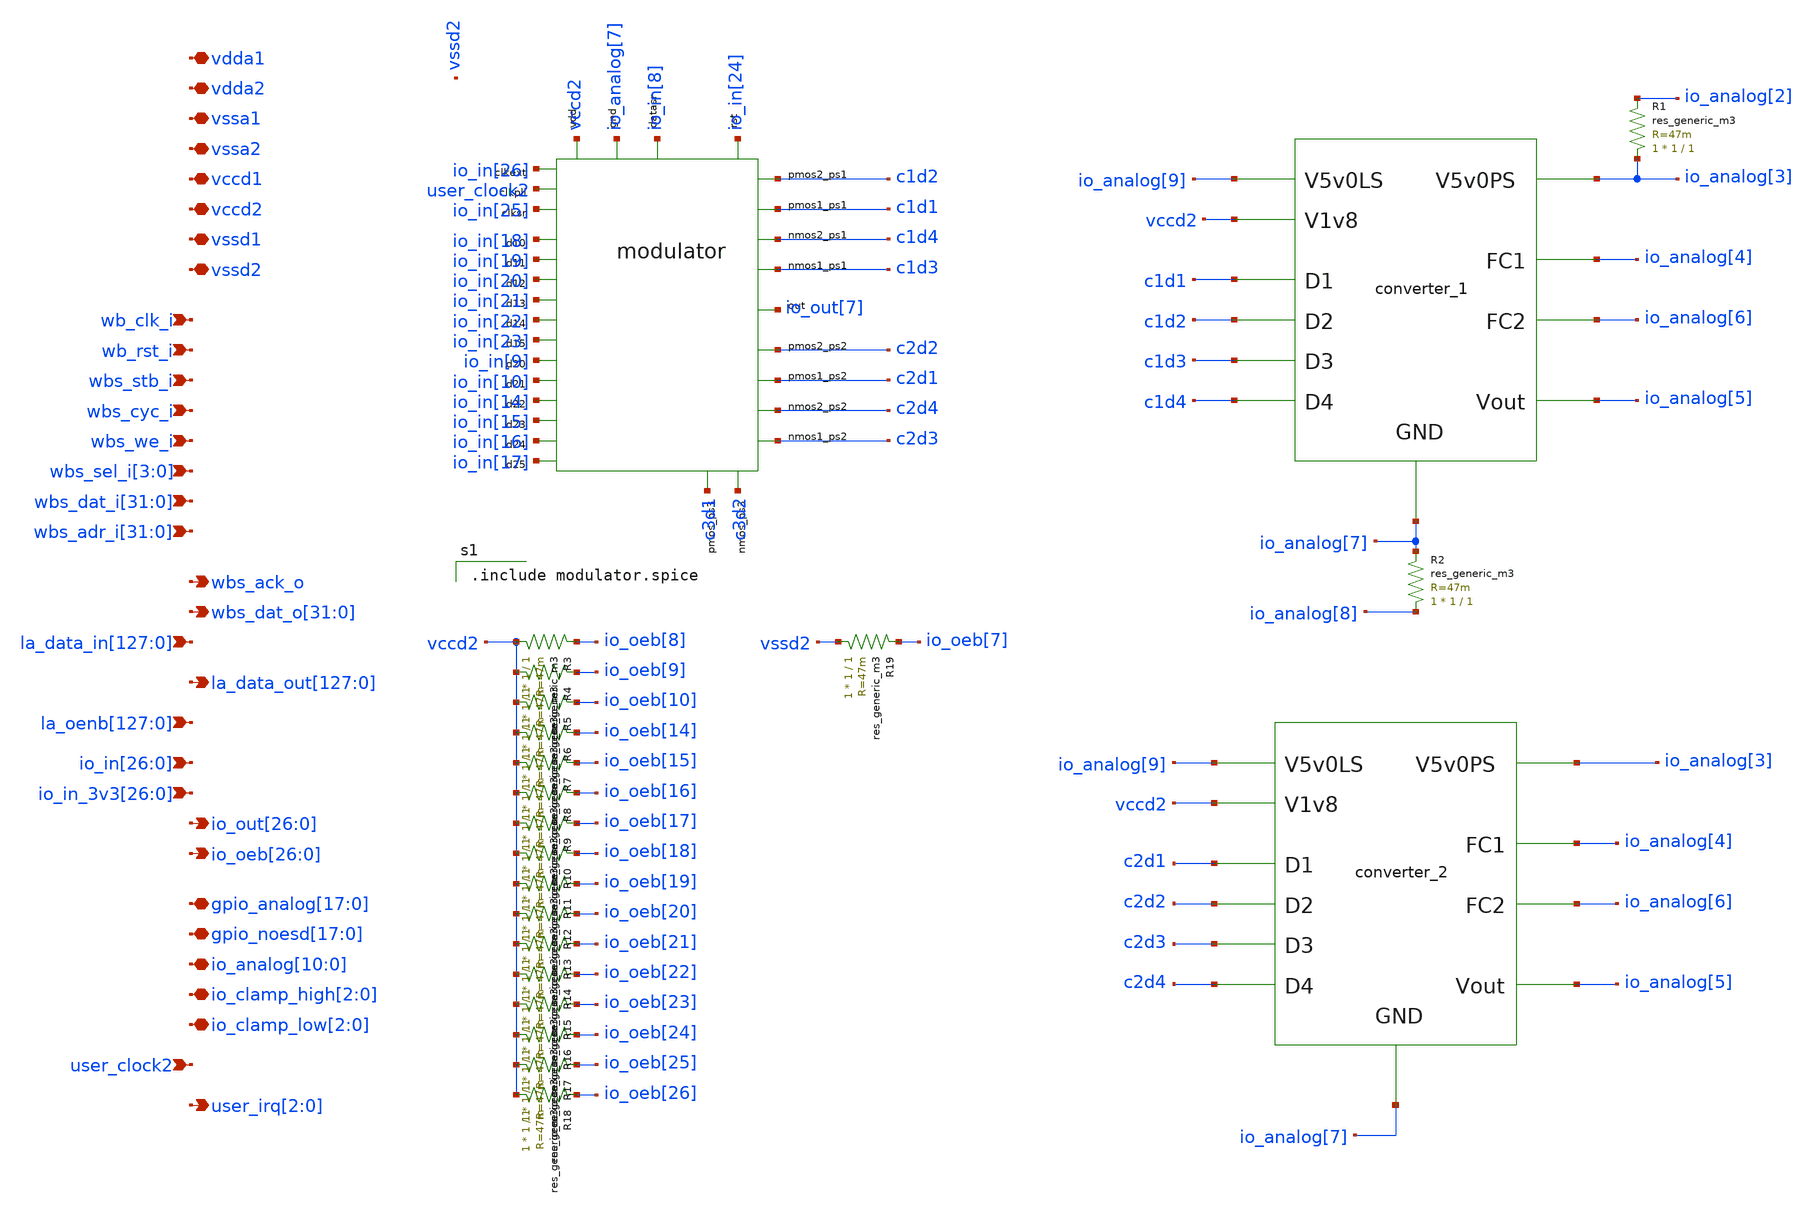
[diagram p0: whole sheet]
** sch_path: user_analog_project_wrapper.sch
**.subckt user_analog_project_wrapper vdda1 vdda2 vssa1 vssa2 vccd1 vccd2 vssd1 vssd2 wb_clk_i
*+ wb_rst_i wbs_stb_i wbs_cyc_i wbs_we_i wbs_sel_i[3],wbs_sel_i[2],wbs_sel_i[1],wbs_sel_i[0]
*+ wbs_dat_i[31],wbs_dat_i[30],wbs_dat_i[29],wbs_dat_i[28],wbs_dat_i[27],wbs_dat_i[26],wbs_dat_i[25],wbs_dat_i[24],wbs_dat_i[23],wbs_dat_i[22],wbs_dat_i[21],wbs_dat_i[20],wbs_dat_i[19],wbs_dat_i[18],wbs_dat_i[17],wbs_dat_i[16],wbs_dat_i[15],wbs_dat_i[14],wbs_dat_i[13],wbs_dat_i[12],wbs_dat_i[11],wbs_dat_i[10],wbs_dat_i[9],wbs_dat_i[8],wbs_dat_i[7],wbs_dat_i[6],wbs_dat_i[5],wbs_dat_i[4],wbs_dat_i[3],wbs_dat_i[2],wbs_dat_i[1],wbs_dat_i[0]
*+ wbs_adr_i[31],wbs_adr_i[30],wbs_adr_i[29],wbs_adr_i[28],wbs_adr_i[27],wbs_adr_i[26],wbs_adr_i[25],wbs_adr_i[24],wbs_adr_i[23],wbs_adr_i[22],wbs_adr_i[21],wbs_adr_i[20],wbs_adr_i[19],wbs_adr_i[18],wbs_adr_i[17],wbs_adr_i[16],wbs_adr_i[15],wbs_adr_i[14],wbs_adr_i[13],wbs_adr_i[12],wbs_adr_i[11],wbs_adr_i[10],wbs_adr_i[9],wbs_adr_i[8],wbs_adr_i[7],wbs_adr_i[6],wbs_adr_i[5],wbs_adr_i[4],wbs_adr_i[3],wbs_adr_i[2],wbs_adr_i[1],wbs_adr_i[0] wbs_ack_o
*+ wbs_dat_o[31],wbs_dat_o[30],wbs_dat_o[29],wbs_dat_o[28],wbs_dat_o[27],wbs_dat_o[26],wbs_dat_o[25],wbs_dat_o[24],wbs_dat_o[23],wbs_dat_o[22],wbs_dat_o[21],wbs_dat_o[20],wbs_dat_o[19],wbs_dat_o[18],wbs_dat_o[17],wbs_dat_o[16],wbs_dat_o[15],wbs_dat_o[14],wbs_dat_o[13],wbs_dat_o[12],wbs_dat_o[11],wbs_dat_o[10],wbs_dat_o[9],wbs_dat_o[8],wbs_dat_o[7],wbs_dat_o[6],wbs_dat_o[5],wbs_dat_o[4],wbs_dat_o[3],wbs_dat_o[2],wbs_dat_o[1],wbs_dat_o[0]
*+ la_data_in[127],la_data_in[126],la_data_in[125],la_data_in[124],la_data_in[123],la_data_in[122],la_data_in[121],la_data_in[120],la_data_in[119],la_data_in[118],la_data_in[117],la_data_in[116],la_data_in[115],la_data_in[114],la_data_in[113],la_data_in[112],la_data_in[111],la_data_in[110],la_data_in[109],la_data_in[108],la_data_in[107],la_data_in[106],la_data_in[105],la_data_in[104],la_data_in[103],la_data_in[102],la_data_in[101],la_data_in[100],la_data_in[99],la_data_in[98],la_data_in[97],la_data_in[96],la_data_in[95],la_data_in[94],la_data_in[93],la_data_in[92],la_data_in[91],la_data_in[90],la_data_in[89],la_data_in[88],la_data_in[87],la_data_in[86],la_data_in[85],la_data_in[84],la_data_in[83],la_data_in[82],la_data_in[81],la_data_in[80],la_data_in[79],la_data_in[78],la_data_in[77],la_data_in[76],la_data_in[75],la_data_in[74],la_data_in[73],la_data_in[72],la_data_in[71],la_data_in[70],la_data_in[69],la_data_in[68],la_data_in[67],la_data_in[66],la_data_in[65],la_data_in[64],la_data_in[63],la_data_in[62],la_data_in[61],la_data_in[60],la_data_in[59],la_data_in[58],la_data_in[57],la_data_in[56],la_data_in[55],la_data_in[54],la_data_in[53],la_data_in[52],la_data_in[51],la_data_in[50],la_data_in[49],la_data_in[48],la_data_in[47],la_data_in[46],la_data_in[45],la_data_in[44],la_data_in[43],la_data_in[42],la_data_in[41],la_data_in[40],la_data_in[39],la_data_in[38],la_data_in[37],la_data_in[36],la_data_in[35],la_data_in[34],la_data_in[33],la_data_in[32],la_data_in[31],la_data_in[30],la_data_in[29],la_data_in[28],la_data_in[27],la_data_in[26],la_data_in[25],la_data_in[24],la_data_in[23],la_data_in[22],la_data_in[21],la_data_in[20],la_data_in[19],la_data_in[18],la_data_in[17],la_data_in[16],la_data_in[15],la_data_in[14],la_data_in[13],la_data_in[12],la_data_in[11],la_data_in[10],la_data_in[9],la_data_in[8],la_data_in[7],la_data_in[6],la_data_in[5],la_data_in[4],la_data_in[3],la_data_in[2],la_data_in[1],la_data_in[0]
*+ la_data_out[127],la_data_out[126],la_data_out[125],la_data_out[124],la_data_out[123],la_data_out[122],la_data_out[121],la_data_out[120],la_data_out[119],la_data_out[118],la_data_out[117],la_data_out[116],la_data_out[115],la_data_out[114],la_data_out[113],la_data_out[112],la_data_out[111],la_data_out[110],la_data_out[109],la_data_out[108],la_data_out[107],la_data_out[106],la_data_out[105],la_data_out[104],la_data_out[103],la_data_out[102],la_data_out[101],la_data_out[100],la_data_out[99],la_data_out[98],la_data_out[97],la_data_out[96],la_data_out[95],la_data_out[94],la_data_out[93],la_data_out[92],la_data_out[91],la_data_out[90],la_data_out[89],la_data_out[88],la_data_out[87],la_data_out[86],la_data_out[85],la_data_out[84],la_data_out[83],la_data_out[82],la_data_out[81],la_data_out[80],la_data_out[79],la_data_out[78],la_data_out[77],la_data_out[76],la_data_out[75],la_data_out[74],la_data_out[73],la_data_out[72],la_data_out[71],la_data_out[70],la_data_out[69],la_data_out[68],la_data_out[67],la_data_out[66],la_data_out[65],la_data_out[64],la_data_out[63],la_data_out[62],la_data_out[61],la_data_out[60],la_data_out[59],la_data_out[58],la_data_out[57],la_data_out[56],la_data_out[55],la_data_out[54],la_data_out[53],la_data_out[52],la_data_out[51],la_data_out[50],la_data_out[49],la_data_out[48],la_data_out[47],la_data_out[46],la_data_out[45],la_data_out[44],la_data_out[43],la_data_out[42],la_data_out[41],la_data_out[40],la_data_out[39],la_data_out[38],la_data_out[37],la_data_out[36],la_data_out[35],la_data_out[34],la_data_out[33],la_data_out[32],la_data_out[31],la_data_out[30],la_data_out[29],la_data_out[28],la_data_out[27],la_data_out[26],la_data_out[25],la_data_out[24],la_data_out[23],la_data_out[22],la_data_out[21],la_data_out[20],la_data_out[19],la_data_out[18],la_data_out[17],la_data_out[16],la_data_out[15],la_data_out[14],la_data_out[13],la_data_out[12],la_data_out[11],la_data_out[10],la_data_out[9],la_data_out[8],la_data_out[7],la_data_out[6],la_data_out[5],la_data_out[4],la_data_out[3],la_data_out[2],la_data_out[1],la_data_out[0]
*+ io_in[26],io_in[25],io_in[24],io_in[23],io_in[22],io_in[21],io_in[20],io_in[19],io_in[18],io_in[17],io_in[16],io_in[15],io_in[14],io_in[13],io_in[12],io_in[11],io_in[10],io_in[9],io_in[8],io_in[7],io_in[6],io_in[5],io_in[4],io_in[3],io_in[2],io_in[1],io_in[0]
*+ io_in_3v3[26],io_in_3v3[25],io_in_3v3[24],io_in_3v3[23],io_in_3v3[22],io_in_3v3[21],io_in_3v3[20],io_in_3v3[19],io_in_3v3[18],io_in_3v3[17],io_in_3v3[16],io_in_3v3[15],io_in_3v3[14],io_in_3v3[13],io_in_3v3[12],io_in_3v3[11],io_in_3v3[10],io_in_3v3[9],io_in_3v3[8],io_in_3v3[7],io_in_3v3[6],io_in_3v3[5],io_in_3v3[4],io_in_3v3[3],io_in_3v3[2],io_in_3v3[1],io_in_3v3[0] user_clock2
*+ io_out[26],io_out[25],io_out[24],io_out[23],io_out[22],io_out[21],io_out[20],io_out[19],io_out[18],io_out[17],io_out[16],io_out[15],io_out[14],io_out[13],io_out[12],io_out[11],io_out[10],io_out[9],io_out[8],io_out[7],io_out[6],io_out[5],io_out[4],io_out[3],io_out[2],io_out[1],io_out[0]
*+ io_oeb[26],io_oeb[25],io_oeb[24],io_oeb[23],io_oeb[22],io_oeb[21],io_oeb[20],io_oeb[19],io_oeb[18],io_oeb[17],io_oeb[16],io_oeb[15],io_oeb[14],io_oeb[13],io_oeb[12],io_oeb[11],io_oeb[10],io_oeb[9],io_oeb[8],io_oeb[7],io_oeb[6],io_oeb[5],io_oeb[4],io_oeb[3],io_oeb[2],io_oeb[1],io_oeb[0]
*+ gpio_analog[17],gpio_analog[16],gpio_analog[15],gpio_analog[14],gpio_analog[13],gpio_analog[12],gpio_analog[11],gpio_analog[10],gpio_analog[9],gpio_analog[8],gpio_analog[7],gpio_analog[6],gpio_analog[5],gpio_analog[4],gpio_analog[3],gpio_analog[2],gpio_analog[1],gpio_analog[0]
*+ gpio_noesd[17],gpio_noesd[16],gpio_noesd[15],gpio_noesd[14],gpio_noesd[13],gpio_noesd[12],gpio_noesd[11],gpio_noesd[10],gpio_noesd[9],gpio_noesd[8],gpio_noesd[7],gpio_noesd[6],gpio_noesd[5],gpio_noesd[4],gpio_noesd[3],gpio_noesd[2],gpio_noesd[1],gpio_noesd[0]
*+ io_analog[10],io_analog[9],io_analog[8],io_analog[7],io_analog[6],io_analog[5],io_analog[4],io_analog[3],io_analog[2],io_analog[1],io_analog[0] io_clamp_high[2],io_clamp_high[1],io_clamp_high[0] io_clamp_low[2],io_clamp_low[1],io_clamp_low[0]
*+ user_irq[2],user_irq[1],user_irq[0]
*+ la_oenb[127],la_oenb[126],la_oenb[125],la_oenb[124],la_oenb[123],la_oenb[122],la_oenb[121],la_oenb[120],la_oenb[119],la_oenb[118],la_oenb[117],la_oenb[116],la_oenb[115],la_oenb[114],la_oenb[113],la_oenb[112],la_oenb[111],la_oenb[110],la_oenb[109],la_oenb[108],la_oenb[107],la_oenb[106],la_oenb[105],la_oenb[104],la_oenb[103],la_oenb[102],la_oenb[101],la_oenb[100],la_oenb[99],la_oenb[98],la_oenb[97],la_oenb[96],la_oenb[95],la_oenb[94],la_oenb[93],la_oenb[92],la_oenb[91],la_oenb[90],la_oenb[89],la_oenb[88],la_oenb[87],la_oenb[86],la_oenb[85],la_oenb[84],la_oenb[83],la_oenb[82],la_oenb[81],la_oenb[80],la_oenb[79],la_oenb[78],la_oenb[77],la_oenb[76],la_oenb[75],la_oenb[74],la_oenb[73],la_oenb[72],la_oenb[71],la_oenb[70],la_oenb[69],la_oenb[68],la_oenb[67],la_oenb[66],la_oenb[65],la_oenb[64],la_oenb[63],la_oenb[62],la_oenb[61],la_oenb[60],la_oenb[59],la_oenb[58],la_oenb[57],la_oenb[56],la_oenb[55],la_oenb[54],la_oenb[53],la_oenb[52],la_oenb[51],la_oenb[50],la_oenb[49],la_oenb[48],la_oenb[47],la_oenb[46],la_oenb[45],la_oenb[44],la_oenb[43],la_oenb[42],la_oenb[41],la_oenb[40],la_oenb[39],la_oenb[38],la_oenb[37],la_oenb[36],la_oenb[35],la_oenb[34],la_oenb[33],la_oenb[32],la_oenb[31],la_oenb[30],la_oenb[29],la_oenb[28],la_oenb[27],la_oenb[26],la_oenb[25],la_oenb[24],la_oenb[23],la_oenb[22],la_oenb[21],la_oenb[20],la_oenb[19],la_oenb[18],la_oenb[17],la_oenb[16],la_oenb[15],la_oenb[14],la_oenb[13],la_oenb[12],la_oenb[11],la_oenb[10],la_oenb[9],la_oenb[8],la_oenb[7],la_oenb[6],la_oenb[5],la_oenb[4],la_oenb[3],la_oenb[2],la_oenb[1],la_oenb[0]
*.iopin vdda1
*.iopin vdda2
*.iopin vssa1
*.iopin vssa2
*.iopin vccd1
*.iopin vccd2
*.iopin vssd1
*.iopin vssd2
*.ipin wb_clk_i
*.ipin wb_rst_i
*.ipin wbs_stb_i
*.ipin wbs_cyc_i
*.ipin wbs_we_i
*.ipin wbs_sel_i[3],wbs_sel_i[2],wbs_sel_i[1],wbs_sel_i[0]
*.ipin
*+ wbs_dat_i[31],wbs_dat_i[30],wbs_dat_i[29],wbs_dat_i[28],wbs_dat_i[27],wbs_dat_i[26],wbs_dat_i[25],wbs_dat_i[24],wbs_dat_i[23],wbs_dat_i[22],wbs_dat_i[21],wbs_dat_i[20],wbs_dat_i[19],wbs_dat_i[18],wbs_dat_i[17],wbs_dat_i[16],wbs_dat_i[15],wbs_dat_i[14],wbs_dat_i[13],wbs_dat_i[12],wbs_dat_i[11],wbs_dat_i[10],wbs_dat_i[9],wbs_dat_i[8],wbs_dat_i[7],wbs_dat_i[6],wbs_dat_i[5],wbs_dat_i[4],wbs_dat_i[3],wbs_dat_i[2],wbs_dat_i[1],wbs_dat_i[0]
*.ipin
*+ wbs_adr_i[31],wbs_adr_i[30],wbs_adr_i[29],wbs_adr_i[28],wbs_adr_i[27],wbs_adr_i[26],wbs_adr_i[25],wbs_adr_i[24],wbs_adr_i[23],wbs_adr_i[22],wbs_adr_i[21],wbs_adr_i[20],wbs_adr_i[19],wbs_adr_i[18],wbs_adr_i[17],wbs_adr_i[16],wbs_adr_i[15],wbs_adr_i[14],wbs_adr_i[13],wbs_adr_i[12],wbs_adr_i[11],wbs_adr_i[10],wbs_adr_i[9],wbs_adr_i[8],wbs_adr_i[7],wbs_adr_i[6],wbs_adr_i[5],wbs_adr_i[4],wbs_adr_i[3],wbs_adr_i[2],wbs_adr_i[1],wbs_adr_i[0]
*.opin wbs_ack_o
*.opin
*+ wbs_dat_o[31],wbs_dat_o[30],wbs_dat_o[29],wbs_dat_o[28],wbs_dat_o[27],wbs_dat_o[26],wbs_dat_o[25],wbs_dat_o[24],wbs_dat_o[23],wbs_dat_o[22],wbs_dat_o[21],wbs_dat_o[20],wbs_dat_o[19],wbs_dat_o[18],wbs_dat_o[17],wbs_dat_o[16],wbs_dat_o[15],wbs_dat_o[14],wbs_dat_o[13],wbs_dat_o[12],wbs_dat_o[11],wbs_dat_o[10],wbs_dat_o[9],wbs_dat_o[8],wbs_dat_o[7],wbs_dat_o[6],wbs_dat_o[5],wbs_dat_o[4],wbs_dat_o[3],wbs_dat_o[2],wbs_dat_o[1],wbs_dat_o[0]
*.ipin
*+ la_data_in[127],la_data_in[126],la_data_in[125],la_data_in[124],la_data_in[123],la_data_in[122],la_data_in[121],la_data_in[120],la_data_in[119],la_data_in[118],la_data_in[117],la_data_in[116],la_data_in[115],la_data_in[114],la_data_in[113],la_data_in[112],la_data_in[111],la_data_in[110],la_data_in[109],la_data_in[108],la_data_in[107],la_data_in[106],la_data_in[105],la_data_in[104],la_data_in[103],la_data_in[102],la_data_in[101],la_data_in[100],la_data_in[99],la_data_in[98],la_data_in[97],la_data_in[96],la_data_in[95],la_data_in[94],la_data_in[93],la_data_in[92],la_data_in[91],la_data_in[90],la_data_in[89],la_data_in[88],la_data_in[87],la_data_in[86],la_data_in[85],la_data_in[84],la_data_in[83],la_data_in[82],la_data_in[81],la_data_in[80],la_data_in[79],la_data_in[78],la_data_in[77],la_data_in[76],la_data_in[75],la_data_in[74],la_data_in[73],la_data_in[72],la_data_in[71],la_data_in[70],la_data_in[69],la_data_in[68],la_data_in[67],la_data_in[66],la_data_in[65],la_data_in[64],la_data_in[63],la_data_in[62],la_data_in[61],la_data_in[60],la_data_in[59],la_data_in[58],la_data_in[57],la_data_in[56],la_data_in[55],la_data_in[54],la_data_in[53],la_data_in[52],la_data_in[51],la_data_in[50],la_data_in[49],la_data_in[48],la_data_in[47],la_data_in[46],la_data_in[45],la_data_in[44],la_data_in[43],la_data_in[42],la_data_in[41],la_data_in[40],la_data_in[39],la_data_in[38],la_data_in[37],la_data_in[36],la_data_in[35],la_data_in[34],la_data_in[33],la_data_in[32],la_data_in[31],la_data_in[30],la_data_in[29],la_data_in[28],la_data_in[27],la_data_in[26],la_data_in[25],la_data_in[24],la_data_in[23],la_data_in[22],la_data_in[21],la_data_in[20],la_data_in[19],la_data_in[18],la_data_in[17],la_data_in[16],la_data_in[15],la_data_in[14],la_data_in[13],la_data_in[12],la_data_in[11],la_data_in[10],la_data_in[9],la_data_in[8],la_data_in[7],la_data_in[6],la_data_in[5],la_data_in[4],la_data_in[3],la_data_in[2],la_data_in[1],la_data_in[0]
*.opin
*+ la_data_out[127],la_data_out[126],la_data_out[125],la_data_out[124],la_data_out[123],la_data_out[122],la_data_out[121],la_data_out[120],la_data_out[119],la_data_out[118],la_data_out[117],la_data_out[116],la_data_out[115],la_data_out[114],la_data_out[113],la_data_out[112],la_data_out[111],la_data_out[110],la_data_out[109],la_data_out[108],la_data_out[107],la_data_out[106],la_data_out[105],la_data_out[104],la_data_out[103],la_data_out[102],la_data_out[101],la_data_out[100],la_data_out[99],la_data_out[98],la_data_out[97],la_data_out[96],la_data_out[95],la_data_out[94],la_data_out[93],la_data_out[92],la_data_out[91],la_data_out[90],la_data_out[89],la_data_out[88],la_data_out[87],la_data_out[86],la_data_out[85],la_data_out[84],la_data_out[83],la_data_out[82],la_data_out[81],la_data_out[80],la_data_out[79],la_data_out[78],la_data_out[77],la_data_out[76],la_data_out[75],la_data_out[74],la_data_out[73],la_data_out[72],la_data_out[71],la_data_out[70],la_data_out[69],la_data_out[68],la_data_out[67],la_data_out[66],la_data_out[65],la_data_out[64],la_data_out[63],la_data_out[62],la_data_out[61],la_data_out[60],la_data_out[59],la_data_out[58],la_data_out[57],la_data_out[56],la_data_out[55],la_data_out[54],la_data_out[53],la_data_out[52],la_data_out[51],la_data_out[50],la_data_out[49],la_data_out[48],la_data_out[47],la_data_out[46],la_data_out[45],la_data_out[44],la_data_out[43],la_data_out[42],la_data_out[41],la_data_out[40],la_data_out[39],la_data_out[38],la_data_out[37],la_data_out[36],la_data_out[35],la_data_out[34],la_data_out[33],la_data_out[32],la_data_out[31],la_data_out[30],la_data_out[29],la_data_out[28],la_data_out[27],la_data_out[26],la_data_out[25],la_data_out[24],la_data_out[23],la_data_out[22],la_data_out[21],la_data_out[20],la_data_out[19],la_data_out[18],la_data_out[17],la_data_out[16],la_data_out[15],la_data_out[14],la_data_out[13],la_data_out[12],la_data_out[11],la_data_out[10],la_data_out[9],la_data_out[8],la_data_out[7],la_data_out[6],la_data_out[5],la_data_out[4],la_data_out[3],la_data_out[2],la_data_out[1],la_data_out[0]
*.ipin
*+ io_in[26],io_in[25],io_in[24],io_in[23],io_in[22],io_in[21],io_in[20],io_in[19],io_in[18],io_in[17],io_in[16],io_in[15],io_in[14],io_in[13],io_in[12],io_in[11],io_in[10],io_in[9],io_in[8],io_in[7],io_in[6],io_in[5],io_in[4],io_in[3],io_in[2],io_in[1],io_in[0]
*.ipin
*+ io_in_3v3[26],io_in_3v3[25],io_in_3v3[24],io_in_3v3[23],io_in_3v3[22],io_in_3v3[21],io_in_3v3[20],io_in_3v3[19],io_in_3v3[18],io_in_3v3[17],io_in_3v3[16],io_in_3v3[15],io_in_3v3[14],io_in_3v3[13],io_in_3v3[12],io_in_3v3[11],io_in_3v3[10],io_in_3v3[9],io_in_3v3[8],io_in_3v3[7],io_in_3v3[6],io_in_3v3[5],io_in_3v3[4],io_in_3v3[3],io_in_3v3[2],io_in_3v3[1],io_in_3v3[0]
*.ipin user_clock2
*.opin
*+ io_out[26],io_out[25],io_out[24],io_out[23],io_out[22],io_out[21],io_out[20],io_out[19],io_out[18],io_out[17],io_out[16],io_out[15],io_out[14],io_out[13],io_out[12],io_out[11],io_out[10],io_out[9],io_out[8],io_out[7],io_out[6],io_out[5],io_out[4],io_out[3],io_out[2],io_out[1],io_out[0]
*.opin
*+ io_oeb[26],io_oeb[25],io_oeb[24],io_oeb[23],io_oeb[22],io_oeb[21],io_oeb[20],io_oeb[19],io_oeb[18],io_oeb[17],io_oeb[16],io_oeb[15],io_oeb[14],io_oeb[13],io_oeb[12],io_oeb[11],io_oeb[10],io_oeb[9],io_oeb[8],io_oeb[7],io_oeb[6],io_oeb[5],io_oeb[4],io_oeb[3],io_oeb[2],io_oeb[1],io_oeb[0]
*.iopin
*+ gpio_analog[17],gpio_analog[16],gpio_analog[15],gpio_analog[14],gpio_analog[13],gpio_analog[12],gpio_analog[11],gpio_analog[10],gpio_analog[9],gpio_analog[8],gpio_analog[7],gpio_analog[6],gpio_analog[5],gpio_analog[4],gpio_analog[3],gpio_analog[2],gpio_analog[1],gpio_analog[0]
*.iopin
*+ gpio_noesd[17],gpio_noesd[16],gpio_noesd[15],gpio_noesd[14],gpio_noesd[13],gpio_noesd[12],gpio_noesd[11],gpio_noesd[10],gpio_noesd[9],gpio_noesd[8],gpio_noesd[7],gpio_noesd[6],gpio_noesd[5],gpio_noesd[4],gpio_noesd[3],gpio_noesd[2],gpio_noesd[1],gpio_noesd[0]
*.iopin
*+ io_analog[10],io_analog[9],io_analog[8],io_analog[7],io_analog[6],io_analog[5],io_analog[4],io_analog[3],io_analog[2],io_analog[1],io_analog[0]
*.iopin io_clamp_high[2],io_clamp_high[1],io_clamp_high[0]
*.iopin io_clamp_low[2],io_clamp_low[1],io_clamp_low[0]
*.opin user_irq[2],user_irq[1],user_irq[0]
*.ipin
*+ la_oenb[127],la_oenb[126],la_oenb[125],la_oenb[124],la_oenb[123],la_oenb[122],la_oenb[121],la_oenb[120],la_oenb[119],la_oenb[118],la_oenb[117],la_oenb[116],la_oenb[115],la_oenb[114],la_oenb[113],la_oenb[112],la_oenb[111],la_oenb[110],la_oenb[109],la_oenb[108],la_oenb[107],la_oenb[106],la_oenb[105],la_oenb[104],la_oenb[103],la_oenb[102],la_oenb[101],la_oenb[100],la_oenb[99],la_oenb[98],la_oenb[97],la_oenb[96],la_oenb[95],la_oenb[94],la_oenb[93],la_oenb[92],la_oenb[91],la_oenb[90],la_oenb[89],la_oenb[88],la_oenb[87],la_oenb[86],la_oenb[85],la_oenb[84],la_oenb[83],la_oenb[82],la_oenb[81],la_oenb[80],la_oenb[79],la_oenb[78],la_oenb[77],la_oenb[76],la_oenb[75],la_oenb[74],la_oenb[73],la_oenb[72],la_oenb[71],la_oenb[70],la_oenb[69],la_oenb[68],la_oenb[67],la_oenb[66],la_oenb[65],la_oenb[64],la_oenb[63],la_oenb[62],la_oenb[61],la_oenb[60],la_oenb[59],la_oenb[58],la_oenb[57],la_oenb[56],la_oenb[55],la_oenb[54],la_oenb[53],la_oenb[52],la_oenb[51],la_oenb[50],la_oenb[49],la_oenb[48],la_oenb[47],la_oenb[46],la_oenb[45],la_oenb[44],la_oenb[43],la_oenb[42],la_oenb[41],la_oenb[40],la_oenb[39],la_oenb[38],la_oenb[37],la_oenb[36],la_oenb[35],la_oenb[34],la_oenb[33],la_oenb[32],la_oenb[31],la_oenb[30],la_oenb[29],la_oenb[28],la_oenb[27],la_oenb[26],la_oenb[25],la_oenb[24],la_oenb[23],la_oenb[22],la_oenb[21],la_oenb[20],la_oenb[19],la_oenb[18],la_oenb[17],la_oenb[16],la_oenb[15],la_oenb[14],la_oenb[13],la_oenb[12],la_oenb[11],la_oenb[10],la_oenb[9],la_oenb[8],la_oenb[7],la_oenb[6],la_oenb[5],la_oenb[4],la_oenb[3],la_oenb[2],la_oenb[1],la_oenb[0]
X1 vccd2 c1d2 c1d1 io_analog[3] io_analog[7] io_analog[5] c1d3 c1d4 io_analog[4] io_analog[6]
+ io_analog[9] converter_1
X2 vccd2 c2d2 c2d1 io_analog[3] io_analog[7] io_analog[5] c2d3 c2d4 io_analog[4] io_analog[6]
+ io_analog[9] converter_2
XMOD1 vccd2 io_analog[7] io_in[26] user_clock2 io_in[25] io_in[8] c1d3 c2d3 c1d4 c2d4 c3d2 c1d1 c2d1
+ c1d2 c2d2 c3d1 io_in[24] io_out[7] io_in[18] io_in[19] io_in[20] io_in[21] io_in[22] io_in[23] io_in[9]
+ io_in[10] io_in[14] io_in[15] io_in[16] io_in[17] Modulator
R1 io_analog[3] io_analog[2] sky130_fd_pr__res_generic_m3 W=1 L=1 m=1
R2 io_analog[8] io_analog[7] sky130_fd_pr__res_generic_m3 W=1 L=1 m=1
R3 vccd2 io_oeb[8] sky130_fd_pr__res_generic_m3 W=1 L=1 m=1
R4 vccd2 io_oeb[9] sky130_fd_pr__res_generic_m3 W=1 L=1 m=1
R5 vccd2 io_oeb[10] sky130_fd_pr__res_generic_m3 W=1 L=1 m=1
R6 vccd2 io_oeb[14] sky130_fd_pr__res_generic_m3 W=1 L=1 m=1
R7 vccd2 io_oeb[15] sky130_fd_pr__res_generic_m3 W=1 L=1 m=1
R8 vccd2 io_oeb[16] sky130_fd_pr__res_generic_m3 W=1 L=1 m=1
R9 vccd2 io_oeb[17] sky130_fd_pr__res_generic_m3 W=1 L=1 m=1
R10 vccd2 io_oeb[18] sky130_fd_pr__res_generic_m3 W=1 L=1 m=1
R11 vccd2 io_oeb[19] sky130_fd_pr__res_generic_m3 W=1 L=1 m=1
R12 vccd2 io_oeb[20] sky130_fd_pr__res_generic_m3 W=1 L=1 m=1
R13 vccd2 io_oeb[21] sky130_fd_pr__res_generic_m3 W=1 L=1 m=1
R14 vccd2 io_oeb[22] sky130_fd_pr__res_generic_m3 W=1 L=1 m=1
R15 vccd2 io_oeb[23] sky130_fd_pr__res_generic_m3 W=1 L=1 m=1
R16 vccd2 io_oeb[24] sky130_fd_pr__res_generic_m3 W=1 L=1 m=1
R17 vccd2 io_oeb[25] sky130_fd_pr__res_generic_m3 W=1 L=1 m=1
R18 vccd2 io_oeb[26] sky130_fd_pr__res_generic_m3 W=1 L=1 m=1
R19 vssd2 io_oeb[7] sky130_fd_pr__res_generic_m3 W=1 L=1 m=1
**** begin user architecture code

.include modulator.spice

**** end user architecture code
**.ends

* expanding   symbol:  converter_1.sym # of pins=11
** sym_path: converter_1.sym
** sch_path: converter_1.sch
.subckt converter_1 V1v8 D2 D1 V5v0PS GND VOUT D3 D4 FC1 FC2 V5v0LS
*.iopin V5v0PS
*.ipin D2
*.ipin D3
*.ipin D4
*.iopin GND
*.iopin V5v0LS
*.iopin FC1
*.iopin FC2
*.iopin V1v8
*.ipin D1
*.iopin VOUT
x4 V5v0LS V1v8 net4 D4 GND level_shifter
x3 V5v0LS V1v8 net3 D3 GND level_shifter
x2 V5v0LS V1v8 net2 D2 GND level_shifter
x1 V5v0LS V1v8 net1 D1 GND level_shifter
X5 net1 net2 net3 net4 FC1 FC2 VOUT V5v0PS GND power_stage_1
.ends


* expanding   symbol:  converter_2.sym # of pins=11
** sym_path: converter_2.sym
** sch_path: converter_2.sch
.subckt converter_2 V1v8 D2 D1 V5v0PS GND VOUT D3 D4 FC1 FC2 V5v0LS
*.iopin V5v0PS
*.ipin D1
*.ipin D2
*.ipin D3
*.ipin D4
*.iopin V1v8
*.iopin GND
*.iopin V5v0LS
*.iopin FC1
*.iopin FC2
*.iopin VOUT
x4 V5v0LS V1v8 net4 D4 GND level_shifter
x3 V5v0LS V1v8 net3 D3 GND level_shifter
x2 V5v0LS V1v8 net2 D2 GND level_shifter
x1 V5v0LS V1v8 net1 D1 GND level_shifter
X5 net1 net2 net3 net4 FC1 FC2 VOUT V5v0PS GND power_stage_2
.ends


* expanding   symbol:  level_shifter.sym # of pins=5
** sym_path: level_shifter.sym
** sch_path: level_shifter.sch
.subckt level_shifter V5v0 V1v8 OUT IN V0v0
*.ipin IN
*.iopin V1v8
*.iopin V5v0
*.opin OUT
*.iopin V0v0
XM11 net1 IN V1v8 V1v8 sky130_fd_pr__pfet_01v8 L=0.15 W=1 nf=1 ad='int((nf+1)/2) * W/nf * 0.29' as='int((nf+2)/2) * W/nf * 0.29'
+ pd='2*int((nf+1)/2) * (W/nf + 0.29)' ps='2*int((nf+2)/2) * (W/nf + 0.29)' nrd='0.29 / W' nrs='0.29 / W'
+ sa=0 sb=0 sd=0 mult=5 m=5
XM12 net1 IN V0v0 V0v0 sky130_fd_pr__nfet_01v8 L=0.15 W=1 nf=1 ad='int((nf+1)/2) * W/nf * 0.29' as='int((nf+2)/2) * W/nf * 0.29'
+ pd='2*int((nf+1)/2) * (W/nf + 0.29)' ps='2*int((nf+2)/2) * (W/nf + 0.29)' nrd='0.29 / W' nrs='0.29 / W'
+ sa=0 sb=0 sd=0 mult=5 m=5
XM15 net2 net3 V5v0 V5v0 sky130_fd_pr__pfet_g5v0d10v5 L=0.5 W=2 nf=1 ad='int((nf+1)/2) * W/nf * 0.29'
+ as='int((nf+2)/2) * W/nf * 0.29' pd='2*int((nf+1)/2) * (W/nf + 0.29)' ps='2*int((nf+2)/2) * (W/nf + 0.29)'
+ nrd='0.29 / W' nrs='0.29 / W' sa=0 sb=0 sd=0 mult=1 m=1
XM14 net3 net2 V5v0 V5v0 sky130_fd_pr__pfet_g5v0d10v5 L=0.5 W=2 nf=1 ad='int((nf+1)/2) * W/nf * 0.29'
+ as='int((nf+2)/2) * W/nf * 0.29' pd='2*int((nf+1)/2) * (W/nf + 0.29)' ps='2*int((nf+2)/2) * (W/nf + 0.29)'
+ nrd='0.29 / W' nrs='0.29 / W' sa=0 sb=0 sd=0 mult=1 m=1
XM16 net4 net2 V5v0 V5v0 sky130_fd_pr__pfet_g5v0d10v5 L=0.5 W=10 nf=1 ad='int((nf+1)/2) * W/nf * 0.29'
+ as='int((nf+2)/2) * W/nf * 0.29' pd='2*int((nf+1)/2) * (W/nf + 0.29)' ps='2*int((nf+2)/2) * (W/nf + 0.29)'
+ nrd='0.29 / W' nrs='0.29 / W' sa=0 sb=0 sd=0 mult=10 m=10
XM18 net2 net1 V0v0 V0v0 sky130_fd_pr__nfet_g5v0d10v5 L=0.5 W=4 nf=1 ad='int((nf+1)/2) * W/nf * 0.29'
+ as='int((nf+2)/2) * W/nf * 0.29' pd='2*int((nf+1)/2) * (W/nf + 0.29)' ps='2*int((nf+2)/2) * (W/nf + 0.29)'
+ nrd='0.29 / W' nrs='0.29 / W' sa=0 sb=0 sd=0 mult=3 m=3
XM13 net3 IN V0v0 V0v0 sky130_fd_pr__nfet_g5v0d10v5 L=0.5 W=4 nf=1 ad='int((nf+1)/2) * W/nf * 0.29' as='int((nf+2)/2) * W/nf * 0.29'
+ pd='2*int((nf+1)/2) * (W/nf + 0.29)' ps='2*int((nf+2)/2) * (W/nf + 0.29)' nrd='0.29 / W' nrs='0.29 / W'
+ sa=0 sb=0 sd=0 mult=3 m=3
XM17 net4 IN V0v0 V0v0 sky130_fd_pr__nfet_g5v0d10v5 L=0.5 W=10 nf=1 ad='int((nf+1)/2) * W/nf * 0.29'
+ as='int((nf+2)/2) * W/nf * 0.29' pd='2*int((nf+1)/2) * (W/nf + 0.29)' ps='2*int((nf+2)/2) * (W/nf + 0.29)'
+ nrd='0.29 / W' nrs='0.29 / W' sa=0 sb=0 sd=0 mult=10 m=10
XM7 OUT net4 V5v0 V5v0 sky130_fd_pr__pfet_g5v0d10v5 L=0.5 W=20 nf=1 ad='int((nf+1)/2) * W/nf * 0.29'
+ as='int((nf+2)/2) * W/nf * 0.29' pd='2*int((nf+1)/2) * (W/nf + 0.29)' ps='2*int((nf+2)/2) * (W/nf + 0.29)'
+ nrd='0.29 / W' nrs='0.29 / W' sa=0 sb=0 sd=0 mult=20 m=20
XM10 OUT net4 V0v0 V0v0 sky130_fd_pr__nfet_g5v0d10v5 L=0.5 W=20 nf=1 ad='int((nf+1)/2) * W/nf * 0.29'
+ as='int((nf+2)/2) * W/nf * 0.29' pd='2*int((nf+1)/2) * (W/nf + 0.29)' ps='2*int((nf+2)/2) * (W/nf + 0.29)'
+ nrd='0.29 / W' nrs='0.29 / W' sa=0 sb=0 sd=0 mult=20 m=20
.ends


* expanding   symbol:  power_stage_1.sym # of pins=9
** sym_path: power_stage_1.sym
** sch_path: power_stage_1.sch
.subckt power_stage_1 S1 S2 S3 S4 FC1 FC2 VOUT VDD VSS
*.iopin VDD
*.ipin S1
*.ipin S2
*.iopin VOUT
*.ipin S3
*.ipin S4
*.iopin VSS
*.iopin FC1
*.iopin FC2
XM2 VOUT S2 FC1 FC1 sky130_fd_pr__pfet_g5v0d10v5 L=0.5 W=4.38 nf=1 ad='int((nf+1)/2) * W/nf * 0.29' as='int((nf+2)/2) * W/nf * 0.29'
+ pd='2*int((nf+1)/2) * (W/nf + 0.29)' ps='2*int((nf+2)/2) * (W/nf + 0.29)' nrd='0.29 / W' nrs='0.29 / W'
+ sa=0 sb=0 sd=0 mult=4512 m=4512
XM1 FC1 S1 VDD VDD sky130_fd_pr__pfet_g5v0d10v5 L=0.5 W=4.38 nf=1 ad='int((nf+1)/2) * W/nf * 0.29' as='int((nf+2)/2) * W/nf * 0.29'
+ pd='2*int((nf+1)/2) * (W/nf + 0.29)' ps='2*int((nf+2)/2) * (W/nf + 0.29)' nrd='0.29 / W' nrs='0.29 / W'
+ sa=0 sb=0 sd=0 mult=4512 m=4512
XM3 VOUT S3 FC2 FC2 sky130_fd_pr__nfet_g5v0d10v5 L=0.5 W=4.38 nf=1 ad='int((nf+1)/2) * W/nf * 0.29' as='int((nf+2)/2) * W/nf * 0.29'
+ pd='2*int((nf+1)/2) * (W/nf + 0.29)' ps='2*int((nf+2)/2) * (W/nf + 0.29)' nrd='0.29 / W' nrs='0.29 / W'
+ sa=0 sb=0 sd=0 mult=1984 m=1984
XM4 FC2 S4 VSS VSS sky130_fd_pr__nfet_g5v0d10v5 L=0.5 W=4.38 nf=1 ad='int((nf+1)/2) * W/nf * 0.29' as='int((nf+2)/2) * W/nf * 0.29'
+ pd='2*int((nf+1)/2) * (W/nf + 0.29)' ps='2*int((nf+2)/2) * (W/nf + 0.29)' nrd='0.29 / W' nrs='0.29 / W'
+ sa=0 sb=0 sd=0 mult=1984 m=1984
.ends


* expanding   symbol:  power_stage_2.sym # of pins=9
** sym_path: power_stage_2.sym
** sch_path: power_stage_2.sch
.subckt power_stage_2 S1 S2 S3 S4 FC1 FC2 VOUT VDD VSS
*.iopin VDD
*.ipin S1
*.ipin S2
*.iopin VOUT
*.ipin S3
*.ipin S4
*.iopin VSS
*.iopin FC1
*.iopin FC2
XM2 VOUT S2 FC1 FC1 sky130_fd_pr__pfet_g5v0d10v5 L=0.5 W=4.38 nf=1 ad='int((nf+1)/2) * W/nf * 0.29' as='int((nf+2)/2) * W/nf * 0.29'
+ pd='2*int((nf+1)/2) * (W/nf + 0.29)' ps='2*int((nf+2)/2) * (W/nf + 0.29)' nrd='0.29 / W' nrs='0.29 / W'
+ sa=0 sb=0 sd=0 mult=3444 m=3444
XM1 FC1 S1 VDD VDD sky130_fd_pr__pfet_g5v0d10v5 L=0.5 W=4.38 nf=1 ad='int((nf+1)/2) * W/nf * 0.29' as='int((nf+2)/2) * W/nf * 0.29'
+ pd='2*int((nf+1)/2) * (W/nf + 0.29)' ps='2*int((nf+2)/2) * (W/nf + 0.29)' nrd='0.29 / W' nrs='0.29 / W'
+ sa=0 sb=0 sd=0 mult=3444 m=3444
XM3 VOUT S3 FC2 FC2 sky130_fd_pr__nfet_g5v0d10v5 L=0.5 W=4.38 nf=1 ad='int((nf+1)/2) * W/nf * 0.29' as='int((nf+2)/2) * W/nf * 0.29'
+ pd='2*int((nf+1)/2) * (W/nf + 0.29)' ps='2*int((nf+2)/2) * (W/nf + 0.29)' nrd='0.29 / W' nrs='0.29 / W'
+ sa=0 sb=0 sd=0 mult=760 m=760
XM4 FC2 S4 VSS VSS sky130_fd_pr__nfet_g5v0d10v5 L=0.5 W=4.38 nf=1 ad='int((nf+1)/2) * W/nf * 0.29' as='int((nf+2)/2) * W/nf * 0.29'
+ pd='2*int((nf+1)/2) * (W/nf + 0.29)' ps='2*int((nf+2)/2) * (W/nf + 0.29)' nrd='0.29 / W' nrs='0.29 / W'
+ sa=0 sb=0 sd=0 mult=760 m=760
.ends

.end
